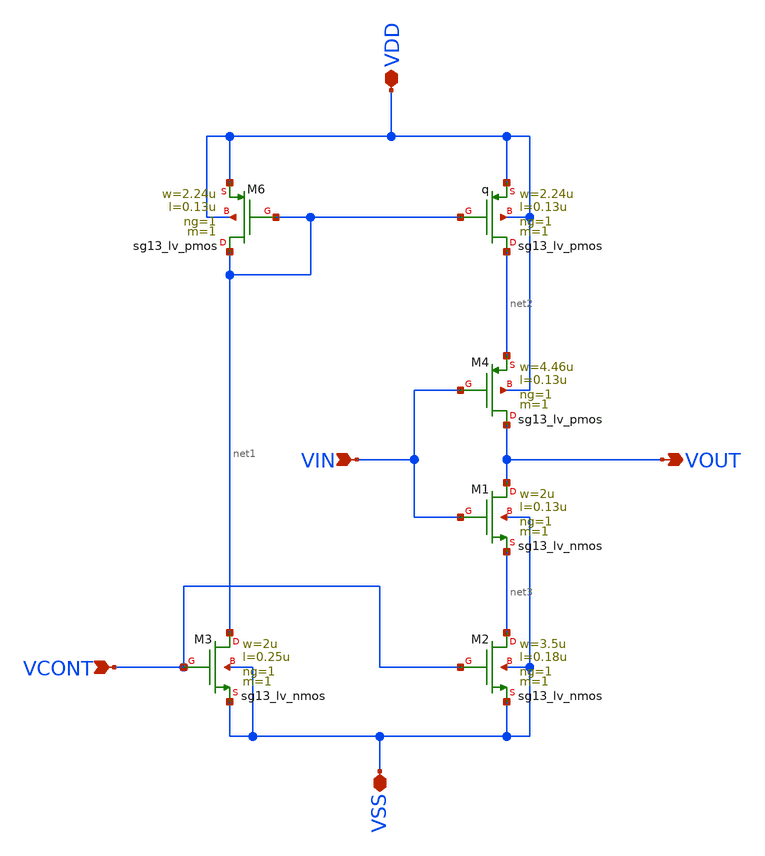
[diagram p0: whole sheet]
** sch_path: unic_cass_wrapper_analog/QDLL/Cells/VCDL.sch
**.subckt VCDL VDD VSS VIN VCONT VOUT
*.iopin VDD
*.iopin VSS
*.ipin VIN
*.ipin VCONT
*.opin VOUT
XM1 VOUT VIN net3 VSS sg13_lv_nmos w=2u l=0.13u ng=1 m=1 mm_ok=1
XM2 net3 VCONT VSS VSS sg13_lv_nmos w=3.5u l=0.18u ng=1 m=1 mm_ok=1
XM3 net1 VCONT VSS VSS sg13_lv_nmos w=2u l=0.25u ng=1 m=1 mm_ok=1
XM4 VOUT VIN net2 VDD sg13_lv_pmos w=4.46u l=0.13u ng=1 m=1 mm_ok=1
Xq net2 net1 VDD VDD sg13_lv_pmos w=2.24u l=0.13u ng=1 m=1 mm_ok=1
XM6 net1 net1 VDD VDD sg13_lv_pmos w=2.24u l=0.13u ng=1 m=1 mm_ok=1
**.ends
.end
